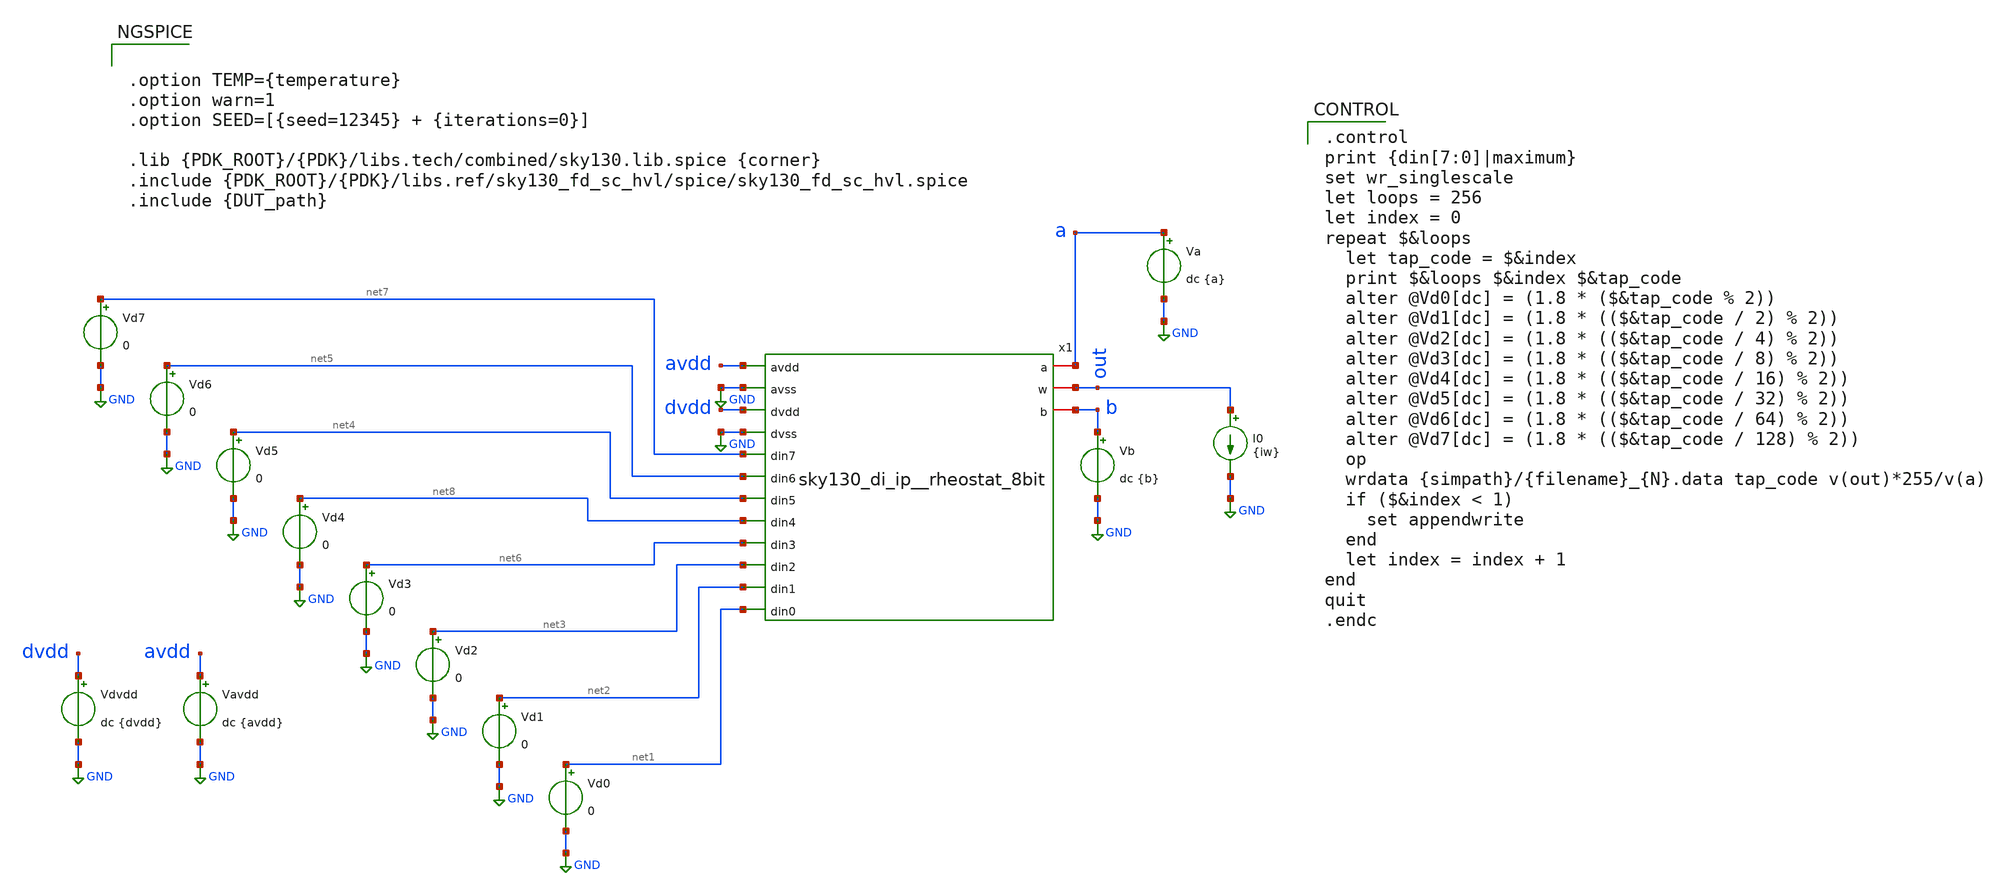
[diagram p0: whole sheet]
** sch_path: cace/tb_dnl.sch
**.subckt tb_dnl
x1 avdd GND dvdd GND net7 net5 net4 a net8 net6 out net3 net2 net1 b sky130_di_ip__rheostat_8bit
Vd0 net1 GND 0
Vd1 net2 GND 0
Vd2 net3 GND 0
Vd3 net6 GND 0
Vd4 net8 GND 0
Vd5 net4 GND 0
Vd6 net5 GND 0
Vd7 net7 GND 0
Vdvdd dvdd GND dc {dvdd}
Vavdd avdd GND dc {avdd}
Va a GND dc {a}
Vb b GND dc {b}
I0 out GND {iw}
**** begin user architecture code


.option TEMP={temperature}
.option warn=1
.option SEED=[{seed=12345} + {iterations=0}]

.lib {PDK_ROOT}/{PDK}/libs.tech/combined/sky130.lib.spice {corner}
.include {PDK_ROOT}/{PDK}/libs.ref/sky130_fd_sc_hvl/spice/sky130_fd_sc_hvl.spice
.include {DUT_path}



.control
print {din[7:0]|maximum}
set wr_singlescale
let loops = 256
let index = 0
repeat $&loops
  let tap_code = $&index
  print $&loops $&index $&tap_code
  alter @Vd0[dc] = (1.8 * ($&tap_code % 2))
  alter @Vd1[dc] = (1.8 * (($&tap_code / 2) % 2))
  alter @Vd2[dc] = (1.8 * (($&tap_code / 4) % 2))
  alter @Vd3[dc] = (1.8 * (($&tap_code / 8) % 2))
  alter @Vd4[dc] = (1.8 * (($&tap_code / 16) % 2))
  alter @Vd5[dc] = (1.8 * (($&tap_code / 32) % 2))
  alter @Vd6[dc] = (1.8 * (($&tap_code / 64) % 2))
  alter @Vd7[dc] = (1.8 * (($&tap_code / 128) % 2))
  op
  wrdata {simpath}/{filename}_{N}.data tap_code v(out)*255/v(a)
  if ($&index < 1)
    set appendwrite
  end
  let index = index + 1
end
quit
.endc


**** end user architecture code
**.ends
.GLOBAL GND
.end
